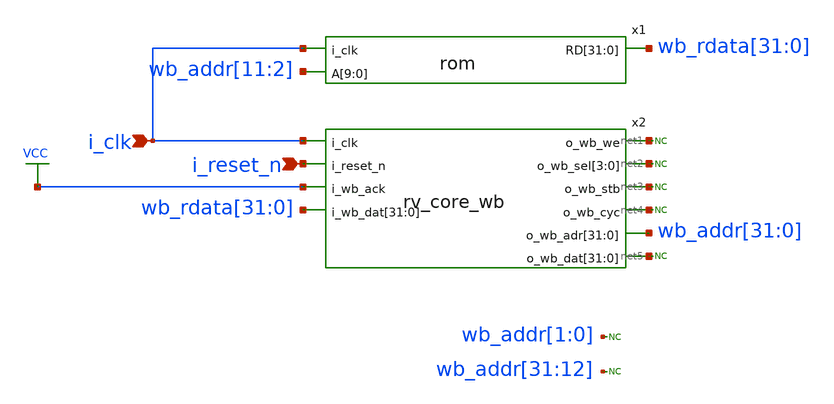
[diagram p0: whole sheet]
** sch_path: blocks/top/top.sch
**.subckt top i_clk i_reset_n
*.ipin i_clk
*.ipin i_reset_n
x1 wb_rdata[31] wb_rdata[30] wb_rdata[29] wb_rdata[28] wb_rdata[27] wb_rdata[26] wb_rdata[25]
+ wb_rdata[24] wb_rdata[23] wb_rdata[22] wb_rdata[21] wb_rdata[20] wb_rdata[19] wb_rdata[18] wb_rdata[17]
+ wb_rdata[16] wb_rdata[15] wb_rdata[14] wb_rdata[13] wb_rdata[12] wb_rdata[11] wb_rdata[10] wb_rdata[9]
+ wb_rdata[8] wb_rdata[7] wb_rdata[6] wb_rdata[5] wb_rdata[4] wb_rdata[3] wb_rdata[2] wb_rdata[1] wb_rdata[0]
+ i_clk wb_addr[11] wb_addr[10] wb_addr[9] wb_addr[8] wb_addr[7] wb_addr[6] wb_addr[5] wb_addr[4]
+ wb_addr[3] wb_addr[2] rom
x2 i_clk net1 i_reset_n net2 net2 net2 net2 VCC net3 wb_rdata[31] wb_rdata[30] wb_rdata[29]
+ wb_rdata[28] wb_rdata[27] wb_rdata[26] wb_rdata[25] wb_rdata[24] wb_rdata[23] wb_rdata[22] wb_rdata[21]
+ wb_rdata[20] wb_rdata[19] wb_rdata[18] wb_rdata[17] wb_rdata[16] wb_rdata[15] wb_rdata[14] wb_rdata[13]
+ wb_rdata[12] wb_rdata[11] wb_rdata[10] wb_rdata[9] wb_rdata[8] wb_rdata[7] wb_rdata[6] wb_rdata[5] wb_rdata[4]
+ wb_rdata[3] wb_rdata[2] wb_rdata[1] wb_rdata[0] net4 wb_addr[31] wb_addr[30] wb_addr[29] wb_addr[28]
+ wb_addr[27] wb_addr[26] wb_addr[25] wb_addr[24] wb_addr[23] wb_addr[22] wb_addr[21] wb_addr[20] wb_addr[19]
+ wb_addr[18] wb_addr[17] wb_addr[16] wb_addr[15] wb_addr[14] wb_addr[13] wb_addr[12] wb_addr[11] wb_addr[10]
+ wb_addr[9] wb_addr[8] wb_addr[7] wb_addr[6] wb_addr[5] wb_addr[4] wb_addr[3] wb_addr[2] wb_addr[1] wb_addr[0]
+ net5 net5 net5 net5 net5 net5 net5 net5 net5 net5 net5 net5 net5 net5 net5 net5 net5 net5 net5 net5 net5
+ net5 net5 net5 net5 net5 net5 net5 net5 net5 net5 net5 rv_core_wb
* noconn #net1
* noconn #net3
* noconn #net4
* noconn #net2
* noconn #net5
* noconn wb_addr[1:0]
* noconn wb_addr[31:12]
**.ends
.GLOBAL VCC
.end
